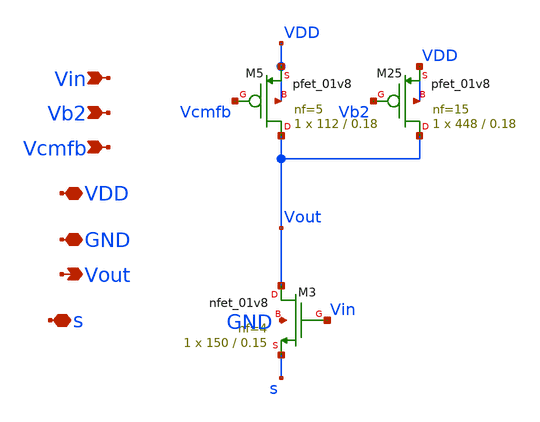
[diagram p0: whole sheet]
** sch_path: schem/core_half.sch
**.subckt core_half Vb2 Vcmfb VDD GND Vout s Vin
*.ipin Vb2
*.ipin Vcmfb
*.iopin VDD
*.iopin GND
*.opin Vout
*.iopin s
*.ipin Vin
XM3 Vout Vin s GND sky130_fd_pr__nfet_01v8 L=0.15 W=150 nf=4 ad='int((nf+1)/2) * W/nf * 0.29' as='int((nf+2)/2) * W/nf * 0.29'
+ pd='2*int((nf+1)/2) * (W/nf + 0.29)' ps='2*int((nf+2)/2) * (W/nf + 0.29)' nrd='0.29 / W' nrs='0.29 / W'
+ sa=0 sb=0 sd=0 mult=1 m=1
XM5 Vout Vcmfb VDD VDD sky130_fd_pr__pfet_01v8 L=0.18 W=112 nf=5 ad='int((nf+1)/2) * W/nf * 0.29' as='int((nf+2)/2) * W/nf * 0.29'
+ pd='2*int((nf+1)/2) * (W/nf + 0.29)' ps='2*int((nf+2)/2) * (W/nf + 0.29)' nrd='0.29 / W' nrs='0.29 / W'
+ sa=0 sb=0 sd=0 mult=1 m=1
XM25 Vout Vb2 VDD VDD sky130_fd_pr__pfet_01v8 L=0.18 W=448 nf=15 ad='int((nf+1)/2) * W/nf * 0.29' as='int((nf+2)/2) * W/nf * 0.29'
+ pd='2*int((nf+1)/2) * (W/nf + 0.29)' ps='2*int((nf+2)/2) * (W/nf + 0.29)' nrd='0.29 / W' nrs='0.29 / W'
+ sa=0 sb=0 sd=0 mult=1 m=1
**.ends
.end
